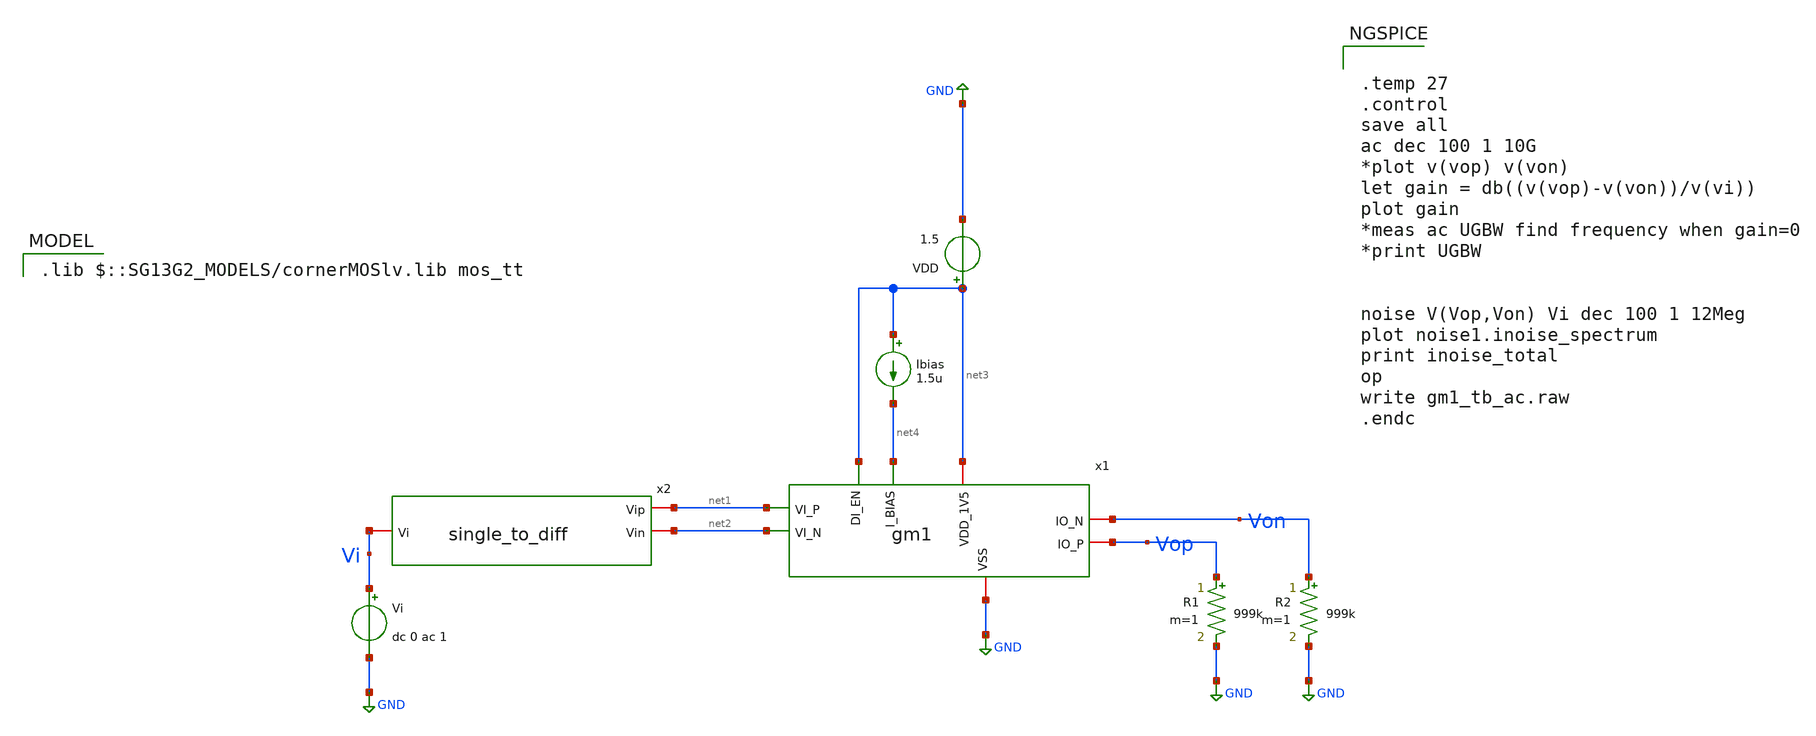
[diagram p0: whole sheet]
** sch_path: gm1_tb_ac.sch
**.subckt gm1_tb_ac
x1 net3 Von Vop net4 net2 net1 net3 GND gm1
x2 net1 net2 Vi single_to_diff
Vi Vi GND dc 0 ac 1
VDD net3 GND 1.5
Ibias net3 net4 1.5u
R1 Vop GND 999k m=1
R2 Von GND 999k m=1
**** begin user architecture code
 .lib $::SG13G2_MODELS/cornerMOSlv.lib mos_tt



.temp 27
.control
save all
ac dec 100 1 10G
*plot v(vop) v(von)
let gain = db((v(vop)-v(von))/v(vi))
plot gain
*meas ac UGBW find frequency when gain=0
*print UGBW


noise V(Vop,Von) Vi dec 100 1 12Meg
plot noise1.inoise_spectrum
print inoise_total
op
write gm1_tb_ac.raw
.endc




.save @n.x1.xm1.nsg13_lv_nmos[gm]
.save @n.x1.xm1.nsg13_lv_nmos[vth]
.save @n.x1.xm1.nsg13_lv_nmos[cgg]
.save @n.x1.xm1.nsg13_lv_nmos[vdss]
.save @n.x1.xm1.nsg13_lv_nmos[ids]
.save @n.x1.xm1.nsg13_lv_nmos[vds]
.save @n.x1.xm1.nsg13_lv_nmos[fug]
.save @n.x1.xm1.nsg13_lv_nmos[vgs]


.save @n.x1.xm2.nsg13_lv_nmos[gm]
.save @n.x1.xm2.nsg13_lv_nmos[vth]
.save @n.x1.xm2.nsg13_lv_nmos[cgg]
.save @n.x1.xm2.nsg13_lv_nmos[vdss]
.save @n.x1.xm2.nsg13_lv_nmos[ids]
.save @n.x1.xm2.nsg13_lv_nmos[vds]
.save @n.x1.xm2.nsg13_lv_nmos[fug]
.save @n.x1.xm2.nsg13_lv_nmos[vgs]


.save @n.x1.xm3.nsg13_lv_pmos[gm]
.save @n.x1.xm3.nsg13_lv_pmos[vth]
.save @n.x1.xm3.nsg13_lv_pmos[cgg]
.save @n.x1.xm3.nsg13_lv_pmos[vdss]
.save @n.x1.xm3.nsg13_lv_pmos[ids]
.save @n.x1.xm3.nsg13_lv_pmos[vds]
.save @n.x1.xm3.nsg13_lv_pmos[fug]
.save @n.x1.xm3.nsg13_lv_pmos[vgs]


.save @n.x1.xm4.nsg13_lv_pmos[gm]
.save @n.x1.xm4.nsg13_lv_pmos[vth]
.save @n.x1.xm4.nsg13_lv_pmos[cgg]
.save @n.x1.xm4.nsg13_lv_pmos[vdss]
.save @n.x1.xm4.nsg13_lv_pmos[ids]
.save @n.x1.xm4.nsg13_lv_pmos[vds]
.save @n.x1.xm4.nsg13_lv_pmos[fug]
.save @n.x1.xm4.nsg13_lv_pmos[vgs]


.save @n.x1.xm5.nsg13_lv_nmos[gm]
.save @n.x1.xm5.nsg13_lv_nmos[vth]
.save @n.x1.xm5.nsg13_lv_nmos[cgg]
.save @n.x1.xm5.nsg13_lv_nmos[vdss]
.save @n.x1.xm5.nsg13_lv_nmos[ids]
.save @n.x1.xm5.nsg13_lv_nmos[vds]
.save @n.x1.xm5.nsg13_lv_nmos[fug]
.save @n.x1.xm5.nsg13_lv_nmos[vgs]


.save @n.x1.xm6.nsg13_lv_nmos[gm]
.save @n.x1.xm6.nsg13_lv_nmos[vth]
.save @n.x1.xm6.nsg13_lv_nmos[cgg]
.save @n.x1.xm6.nsg13_lv_nmos[vdss]
.save @n.x1.xm6.nsg13_lv_nmos[ids]
.save @n.x1.xm6.nsg13_lv_nmos[vds]
.save @n.x1.xm6.nsg13_lv_nmos[fug]
.save @n.x1.xm6.nsg13_lv_nmos[vgs]


.save @n.x1.xm7.nsg13_lv_nmos[gm]
.save @n.x1.xm7.nsg13_lv_nmos[vth]
.save @n.x1.xm7.nsg13_lv_nmos[cgg]
.save @n.x1.xm7.nsg13_lv_nmos[vdss]
.save @n.x1.xm7.nsg13_lv_nmos[ids]
.save @n.x1.xm7.nsg13_lv_nmos[vds]
.save @n.x1.xm7.nsg13_lv_nmos[fug]
.save @n.x1.xm7.nsg13_lv_nmos[vgs]


.save @n.x1.xm8.nsg13_lv_pmos[gm]
.save @n.x1.xm8.nsg13_lv_pmos[vth]
.save @n.x1.xm8.nsg13_lv_pmos[cgg]
.save @n.x1.xm8.nsg13_lv_pmos[vdss]
.save @n.x1.xm8.nsg13_lv_pmos[ids]
.save @n.x1.xm8.nsg13_lv_pmos[vds]
.save @n.x1.xm8.nsg13_lv_pmos[fug]
.save @n.x1.xm8.nsg13_lv_pmos[vgs]


.save @n.x1.xm9.nsg13_lv_nmos[gm]
.save @n.x1.xm9.nsg13_lv_nmos[vth]
.save @n.x1.xm9.nsg13_lv_nmos[cgg]
.save @n.x1.xm9.nsg13_lv_nmos[vdss]
.save @n.x1.xm9.nsg13_lv_nmos[ids]
.save @n.x1.xm9.nsg13_lv_nmos[vds]
.save @n.x1.xm9.nsg13_lv_nmos[fug]
.save @n.x1.xm9.nsg13_lv_nmos[vgs]


.save @n.x1.xm10.nsg13_lv_pmos[gm]
.save @n.x1.xm10.nsg13_lv_pmos[vth]
.save @n.x1.xm10.nsg13_lv_pmos[cgg]
.save @n.x1.xm10.nsg13_lv_pmos[vdss]
.save @n.x1.xm10.nsg13_lv_pmos[ids]
.save @n.x1.xm10.nsg13_lv_pmos[vds]
.save @n.x1.xm10.nsg13_lv_pmos[fug]
.save @n.x1.xm10.nsg13_lv_pmos[vgs]


.save @n.x1.xm11.nsg13_lv_nmos[gm]
.save @n.x1.xm11.nsg13_lv_nmos[vth]
.save @n.x1.xm11.nsg13_lv_nmos[cgg]
.save @n.x1.xm11.nsg13_lv_nmos[vdss]
.save @n.x1.xm11.nsg13_lv_nmos[ids]
.save @n.x1.xm11.nsg13_lv_nmos[vds]
.save @n.x1.xm11.nsg13_lv_nmos[fug]
.save @n.x1.xm11.nsg13_lv_nmos[vgs]


.save @n.x1.xm12.nsg13_lv_nmos[gm]
.save @n.x1.xm12.nsg13_lv_nmos[vth]
.save @n.x1.xm12.nsg13_lv_nmos[cgg]
.save @n.x1.xm12.nsg13_lv_nmos[vdss]
.save @n.x1.xm12.nsg13_lv_nmos[ids]
.save @n.x1.xm12.nsg13_lv_nmos[vds]
.save @n.x1.xm12.nsg13_lv_nmos[fug]
.save @n.x1.xm12.nsg13_lv_nmos[vgs]


.save @n.x1.xm13.nsg13_lv_nmos[gm]
.save @n.x1.xm13.nsg13_lv_nmos[vth]
.save @n.x1.xm13.nsg13_lv_nmos[cgg]
.save @n.x1.xm13.nsg13_lv_nmos[vdss]
.save @n.x1.xm13.nsg13_lv_nmos[ids]
.save @n.x1.xm13.nsg13_lv_nmos[vds]
.save @n.x1.xm13.nsg13_lv_nmos[fug]
.save @n.x1.xm13.nsg13_lv_nmos[vgs]


.save @n.x1.xm14.nsg13_lv_pmos[gm]
.save @n.x1.xm14.nsg13_lv_pmos[vth]
.save @n.x1.xm14.nsg13_lv_pmos[cgg]
.save @n.x1.xm14.nsg13_lv_pmos[vdss]
.save @n.x1.xm14.nsg13_lv_pmos[ids]
.save @n.x1.xm14.nsg13_lv_pmos[vds]
.save @n.x1.xm14.nsg13_lv_pmos[fug]
.save @n.x1.xm14.nsg13_lv_pmos[vgs]


.save @n.x1.xm15.nsg13_lv_pmos[gm]
.save @n.x1.xm15.nsg13_lv_pmos[vth]
.save @n.x1.xm15.nsg13_lv_pmos[cgg]
.save @n.x1.xm15.nsg13_lv_pmos[vdss]
.save @n.x1.xm15.nsg13_lv_pmos[ids]
.save @n.x1.xm15.nsg13_lv_pmos[vds]
.save @n.x1.xm15.nsg13_lv_pmos[fug]
.save @n.x1.xm15.nsg13_lv_pmos[vgs]





**** end user architecture code
**.ends

* expanding   symbol:  gm1.sym # of pins=8
** sym_path: gm1.sym
** sch_path: gm1.sch
.subckt gm1 VDD_1V5 IO_N IO_P I_BIAS VI_N VI_P DI_EN VSS
*.ipin VI_N
*.ipin VI_P
*.iopin VSS
*.iopin VDD_1V5
*.iopin IO_P
*.iopin IO_N
*.ipin I_BIAS
*.ipin DI_EN
XM1 I_drain1 VI_P Vsp Vsp sg13_lv_nmos w=1u l=1u ng=1 m=1 mm_ok=1
XM2 I_drain2 VI_N Vsn Vsn sg13_lv_nmos w=1u l=1u ng=1 m=1 mm_ok=1
R1 Vsp Vsn 600k m=1
XM5 Vsp V_dg VSS VSS sg13_lv_nmos w=0.5u l=1u ng=1 m=1 mm_ok=1
XM6 Vsn V_dg VSS VSS sg13_lv_nmos w=0.5u l=1u ng=1 m=1 mm_ok=1
XM7 V_dg V_dg VSS VSS sg13_lv_nmos w=1u l=1u ng=1 m=1 mm_ok=1
XM8 disable DI_EN VDD_1V5 VDD_1V5 sg13_lv_pmos w=1u l=0.13u ng=1 m=1 mm_ok=1
XM9 enable disable VSS VSS sg13_lv_nmos w=1u l=0.13u ng=1 m=1 mm_ok=1
XM10 enable disable VDD_1V5 VDD_1V5 sg13_lv_pmos w=1u l=0.13u ng=1 m=1 mm_ok=1
XM11 disable DI_EN VSS VSS sg13_lv_nmos w=1u l=0.13u ng=1 m=1 mm_ok=1
XM12 I_BIAS enable V_dg VSS sg13_lv_nmos w=1u l=0.13u ng=1 m=1 mm_ok=1
XM3 I_drain1 I_drain1 VDD_1V5 VDD_1V5 sg13_lv_pmos w=1u l=1u ng=1 m=1 mm_ok=1
XM4 I_drain2 I_drain2 VDD_1V5 VDD_1V5 sg13_lv_pmos w=1u l=1u ng=1 m=1 mm_ok=1
XM14 IO_P I_drain1 VDD_1V5 VDD_1V5 sg13_lv_pmos w=1u l=1u ng=1 m=1 mm_ok=1
XM15 IO_N I_drain2 VDD_1V5 VDD_1V5 sg13_lv_pmos w=1u l=1u ng=1 m=1 mm_ok=1
XM13 V_dg disable VSS VSS sg13_lv_nmos w=1u l=1u ng=1 m=1 mm_ok=1
.ends


* expanding   symbol:  single_to_diff.sym # of pins=3
** sym_path: single_to_diff.sym
** sch_path: single_to_diff.sch
.subckt single_to_diff Vip Vin Vi
*.iopin Vi
*.iopin Vip
*.iopin Vin
E1 net1 GND Vi GND 1
E2 Vin net2 net1 GND -0.5
E3 Vip net2 net1 GND 0.5
Vcm net2 GND 0.75
.ends

.GLOBAL GND
.end
